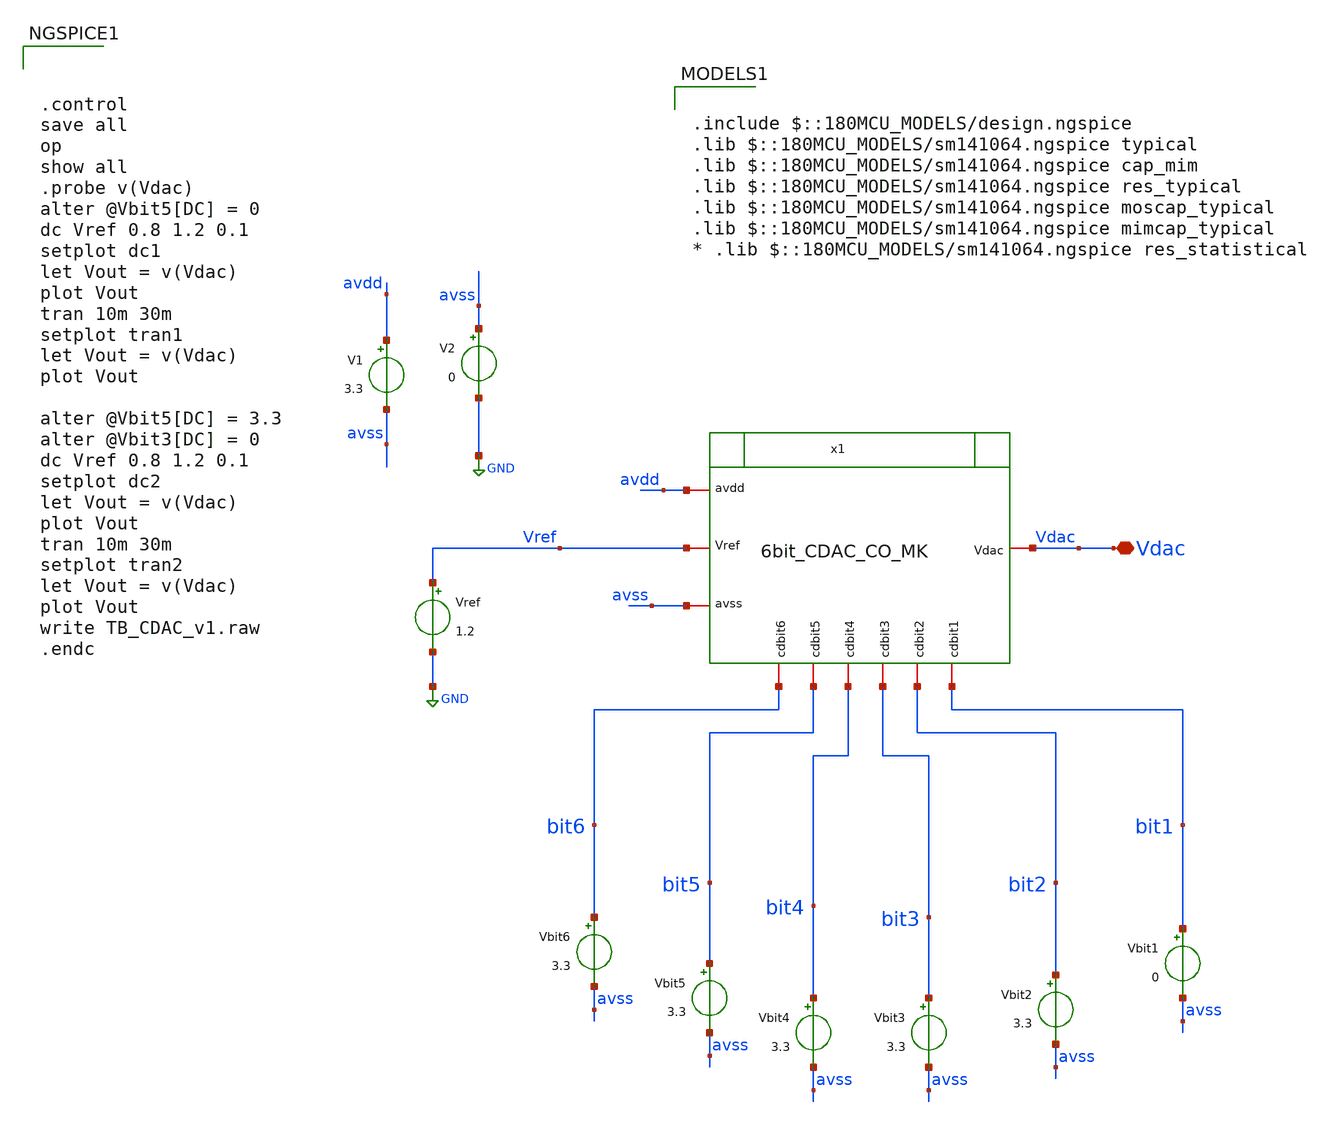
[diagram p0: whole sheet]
** sch_path: designs/libs/WK_Kadam/TB_6bit_CDAC_CO_V1_MK.sch
**.subckt TB_6bit_CDAC_CO_V1_MK Vdac
*.iopin Vdac
x1 Vdac avdd avss Vref bit6 bit5 bit3 bit1 bit2 bit4 6bit_CDAC_CO_MK
V1 avdd avss 3.3
V2 avss GND 0
Vbit1 bit1 avss 0
Vbit2 bit2 avss 3.3
Vbit3 bit3 avss 3.3
Vbit4 bit4 avss 3.3
Vbit5 bit5 avss 3.3
Vbit6 bit6 avss 3.3
Vref Vref GND 1.2
**** begin user architecture code



.control
save all
op
show all
.probe v(Vdac)
alter @Vbit5[DC] = 0
dc Vref 0.8 1.2 0.1
setplot dc1
let Vout = v(Vdac)
plot Vout
tran 10m 30m
setplot tran1
let Vout = v(Vdac)
plot Vout

alter @Vbit5[DC] = 3.3
alter @Vbit3[DC] = 0
dc Vref 0.8 1.2 0.1
setplot dc2
let Vout = v(Vdac)
plot Vout
tran 10m 30m
setplot tran2
let Vout = v(Vdac)
plot Vout
write TB_CDAC_v1.raw
.endc



.include $::180MCU_MODELS/design.ngspice
.lib $::180MCU_MODELS/sm141064.ngspice typical
.lib $::180MCU_MODELS/sm141064.ngspice cap_mim
.lib $::180MCU_MODELS/sm141064.ngspice res_typical
.lib $::180MCU_MODELS/sm141064.ngspice moscap_typical
.lib $::180MCU_MODELS/sm141064.ngspice mimcap_typical
* .lib $::180MCU_MODELS/sm141064.ngspice res_statistical

**** end user architecture code
**.ends

* expanding   symbol:  libs/WK_Kadam/6bit_CDAC_CO_MK.sym # of pins=10
** sym_path: designs/libs/WK_Kadam/6bit_CDAC_CO_MK.sym
** sch_path: designs/libs/WK_Kadam/6bit_CDAC_CO_MK.sch
.subckt 6bit_CDAC_CO_MK Vdac avdd avss Vref cdbit6 cdbit5 cdbit3 cdbit1 cdbit2 cdbit4
*.iopin Vref
*.iopin Vdac
*.iopin avdd
*.iopin avss
*.iopin cdbit6
*.iopin cdbit5
*.iopin cdbit4
*.iopin cdbit3
*.iopin cdbit2
*.iopin cdbit1
XC3 Vdac net2 cap_mim_2f0_m3m4_noshield c_width=10e-6 c_length=10e-6 m=4
XC4 Vdac net3 cap_mim_2f0_m3m4_noshield c_width=10e-6 c_length=10e-6 m=8
XC5 Vdac net4 cap_mim_2f0_m3m4_noshield c_width=10e-6 c_length=10e-6 m=16
XC6 Vdac net5 cap_mim_2f0_m3m4_noshield c_width=10e-6 c_length=10e-6 m=32
XC7 Vdac net6 cap_mim_2f0_m3m4_noshield c_width=10e-6 c_length=10e-6 m=64
x1 avdd avss net6 cdbit6 Vref c_dac1_switch
x2 avdd avss net5 cdbit5 Vref c_dac1_switch
x3 avdd avss net4 cdbit4 Vref c_dac1_switch
x4 avdd avss net3 cdbit3 Vref c_dac1_switch
x5 avdd avss net1 cdbit1 Vref c_dac1_switch
x6 avdd avss net2 cdbit2 Vref c_dac1_switch
XC1 Vdac avss cap_mim_2f0_m3m4_noshield c_width=10e-6 c_length=10e-6 m=2
XC2 Vdac net1 cap_mim_2f0_m3m4_noshield c_width=10e-6 c_length=10e-6 m=2
.ends


* expanding   symbol:  Wk_Chip_Odyssey/designs/libs/WK_Kadam/c_dac1_switch.sym # of pins=5
** sym_path: designs/libs/WK_Kadam/c_dac1_switch.sym
** sch_path: designs/libs/WK_Kadam/c_dac1_switch.sch
.subckt c_dac1_switch avdd avss sw_vout sw_bit sw_Vref
*.iopin avdd
*.iopin avss
*.iopin sw_bit
*.iopin sw_vout
*.iopin sw_Vref
XM1 sw_vout sw_bit sw_Vref avss nfet_03v3 L=0.28u W=2u nf=1 ad='int((nf+1)/2) * W/nf * 0.18u' as='int((nf+2)/2) * W/nf * 0.18u'
+ pd='2*int((nf+1)/2) * (W/nf + 0.18u)' ps='2*int((nf+2)/2) * (W/nf + 0.18u)' nrd='0.18u / W' nrs='0.18u / W'
+ sa=0 sb=0 sd=0 m=1
XM3 sw_vout net1 avss avss nfet_03v3 L=0.28u W=2u nf=1 ad='int((nf+1)/2) * W/nf * 0.18u' as='int((nf+2)/2) * W/nf * 0.18u'
+ pd='2*int((nf+1)/2) * (W/nf + 0.18u)' ps='2*int((nf+2)/2) * (W/nf + 0.18u)' nrd='0.18u / W' nrs='0.18u / W'
+ sa=0 sb=0 sd=0 m=1
XM4 avss sw_bit sw_vout avdd pfet_03v3 L=0.28u W=2u nf=1 ad='int((nf+1)/2) * W/nf * 0.18u' as='int((nf+2)/2) * W/nf * 0.18u'
+ pd='2*int((nf+1)/2) * (W/nf + 0.18u)' ps='2*int((nf+2)/2) * (W/nf + 0.18u)' nrd='0.18u / W' nrs='0.18u / W'
+ sa=0 sb=0 sd=0 m=1
XM2 sw_Vref net1 sw_vout avdd pfet_03v3 L=0.28u W=2u nf=1 ad='int((nf+1)/2) * W/nf * 0.18u' as='int((nf+2)/2) * W/nf * 0.18u'
+ pd='2*int((nf+1)/2) * (W/nf + 0.18u)' ps='2*int((nf+2)/2) * (W/nf + 0.18u)' nrd='0.18u / W' nrs='0.18u / W'
+ sa=0 sb=0 sd=0 m=1
x1v avdd sw_bit net1 avss inv_test
.ends


* expanding   symbol:  libs/WK_Kadam/inv_test.sym # of pins=4
** sym_path: libs/WK_Kadam/inv_test.sym
** sch_path: libs/WK_Kadam/inv_test.sch
.subckt inv_test avdd in out avss
*.iopin avdd
*.iopin avss
*.iopin in
*.iopin out
XM3 out in avss avss nfet_03v3 L=0.28u W=1u nf=1 ad='int((nf+1)/2) * W/nf * 0.18u' as='int((nf+2)/2) * W/nf * 0.18u'
+ pd='2*int((nf+1)/2) * (W/nf + 0.18u)' ps='2*int((nf+2)/2) * (W/nf + 0.18u)' nrd='0.18u / W' nrs='0.18u / W'
+ sa=0 sb=0 sd=0 m=1
XM4 out in avdd avdd pfet_03v3 L=0.28u W=2.5u nf=1 ad='int((nf+1)/2) * W/nf * 0.18u' as='int((nf+2)/2) * W/nf * 0.18u'
+ pd='2*int((nf+1)/2) * (W/nf + 0.18u)' ps='2*int((nf+2)/2) * (W/nf + 0.18u)' nrd='0.18u / W' nrs='0.18u / W'
+ sa=0 sb=0 sd=0 m=1
.ends

.GLOBAL GND
.end
